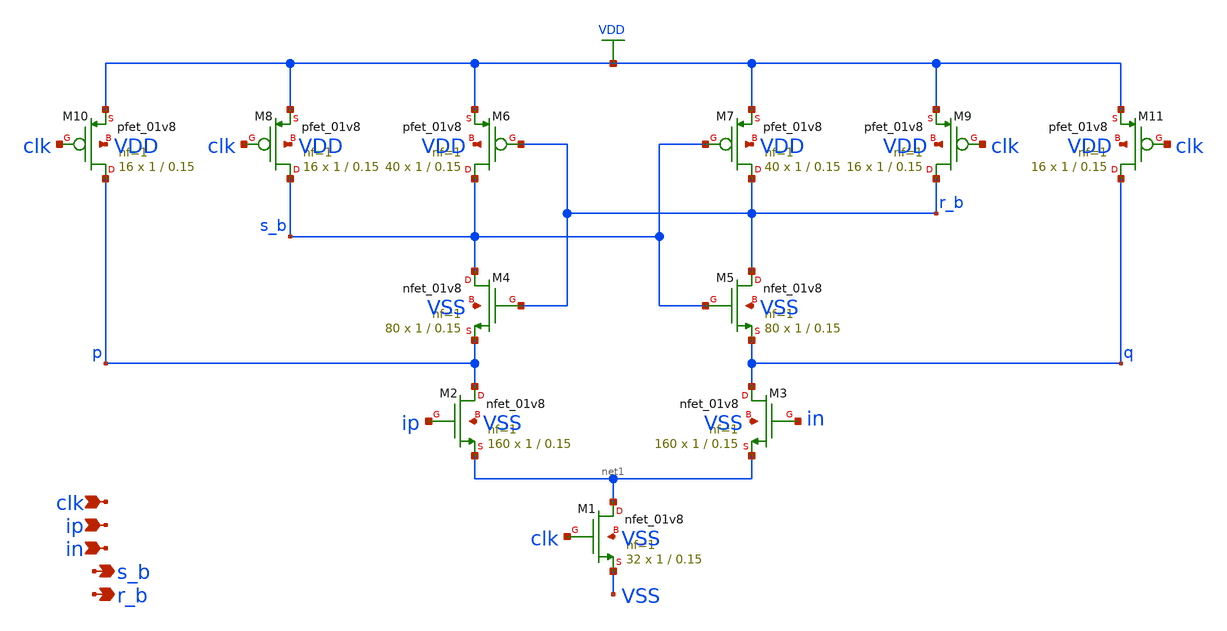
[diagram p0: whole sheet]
** sch_path: design/analog_modulator/schematic/comparator_core_large.sch
**.subckt comparator_core_large clk ip in s_b r_b
*.ipin clk
*.ipin ip
*.ipin in
*.opin s_b
*.opin r_b
XM1 net1 clk VSS VSS sky130_fd_pr__nfet_01v8 L=0.15 W=1 nf=1 ad='int((nf+1)/2) * W/nf * 0.29' as='int((nf+2)/2) * W/nf * 0.29'
+ pd='2*int((nf+1)/2) * (W/nf + 0.29)' ps='2*int((nf+2)/2) * (W/nf + 0.29)' nrd='0.29 / W' nrs='0.29 / W'
+ sa=0 sb=0 sd=0 mult=32 m=32
XM2 p ip net1 VSS sky130_fd_pr__nfet_01v8 L=0.15 W=1 nf=1 ad='int((nf+1)/2) * W/nf * 0.29' as='int((nf+2)/2) * W/nf * 0.29'
+ pd='2*int((nf+1)/2) * (W/nf + 0.29)' ps='2*int((nf+2)/2) * (W/nf + 0.29)' nrd='0.29 / W' nrs='0.29 / W'
+ sa=0 sb=0 sd=0 mult=160 m=160
XM3 q in net1 VSS sky130_fd_pr__nfet_01v8 L=0.15 W=1 nf=1 ad='int((nf+1)/2) * W/nf * 0.29' as='int((nf+2)/2) * W/nf * 0.29'
+ pd='2*int((nf+1)/2) * (W/nf + 0.29)' ps='2*int((nf+2)/2) * (W/nf + 0.29)' nrd='0.29 / W' nrs='0.29 / W'
+ sa=0 sb=0 sd=0 mult=160 m=160
XM4 s_b r_b p VSS sky130_fd_pr__nfet_01v8 L=0.15 W=1 nf=1 ad='int((nf+1)/2) * W/nf * 0.29' as='int((nf+2)/2) * W/nf * 0.29'
+ pd='2*int((nf+1)/2) * (W/nf + 0.29)' ps='2*int((nf+2)/2) * (W/nf + 0.29)' nrd='0.29 / W' nrs='0.29 / W'
+ sa=0 sb=0 sd=0 mult=80 m=80
XM5 r_b s_b q VSS sky130_fd_pr__nfet_01v8 L=0.15 W=1 nf=1 ad='int((nf+1)/2) * W/nf * 0.29' as='int((nf+2)/2) * W/nf * 0.29'
+ pd='2*int((nf+1)/2) * (W/nf + 0.29)' ps='2*int((nf+2)/2) * (W/nf + 0.29)' nrd='0.29 / W' nrs='0.29 / W'
+ sa=0 sb=0 sd=0 mult=80 m=80
XM6 s_b r_b VDD VDD sky130_fd_pr__pfet_01v8 L=0.15 W=1 nf=1 ad='int((nf+1)/2) * W/nf * 0.29' as='int((nf+2)/2) * W/nf * 0.29'
+ pd='2*int((nf+1)/2) * (W/nf + 0.29)' ps='2*int((nf+2)/2) * (W/nf + 0.29)' nrd='0.29 / W' nrs='0.29 / W'
+ sa=0 sb=0 sd=0 mult=40 m=40
XM7 r_b s_b VDD VDD sky130_fd_pr__pfet_01v8 L=0.15 W=1 nf=1 ad='int((nf+1)/2) * W/nf * 0.29' as='int((nf+2)/2) * W/nf * 0.29'
+ pd='2*int((nf+1)/2) * (W/nf + 0.29)' ps='2*int((nf+2)/2) * (W/nf + 0.29)' nrd='0.29 / W' nrs='0.29 / W'
+ sa=0 sb=0 sd=0 mult=40 m=40
XM8 s_b clk VDD VDD sky130_fd_pr__pfet_01v8 L=0.15 W=1 nf=1 ad='int((nf+1)/2) * W/nf * 0.29' as='int((nf+2)/2) * W/nf * 0.29'
+ pd='2*int((nf+1)/2) * (W/nf + 0.29)' ps='2*int((nf+2)/2) * (W/nf + 0.29)' nrd='0.29 / W' nrs='0.29 / W'
+ sa=0 sb=0 sd=0 mult=16 m=16
XM9 r_b clk VDD VDD sky130_fd_pr__pfet_01v8 L=0.15 W=1 nf=1 ad='int((nf+1)/2) * W/nf * 0.29' as='int((nf+2)/2) * W/nf * 0.29'
+ pd='2*int((nf+1)/2) * (W/nf + 0.29)' ps='2*int((nf+2)/2) * (W/nf + 0.29)' nrd='0.29 / W' nrs='0.29 / W'
+ sa=0 sb=0 sd=0 mult=16 m=16
XM10 p clk VDD VDD sky130_fd_pr__pfet_01v8 L=0.15 W=1 nf=1 ad='int((nf+1)/2) * W/nf * 0.29' as='int((nf+2)/2) * W/nf * 0.29'
+ pd='2*int((nf+1)/2) * (W/nf + 0.29)' ps='2*int((nf+2)/2) * (W/nf + 0.29)' nrd='0.29 / W' nrs='0.29 / W'
+ sa=0 sb=0 sd=0 mult=16 m=16
XM11 q clk VDD VDD sky130_fd_pr__pfet_01v8 L=0.15 W=1 nf=1 ad='int((nf+1)/2) * W/nf * 0.29' as='int((nf+2)/2) * W/nf * 0.29'
+ pd='2*int((nf+1)/2) * (W/nf + 0.29)' ps='2*int((nf+2)/2) * (W/nf + 0.29)' nrd='0.29 / W' nrs='0.29 / W'
+ sa=0 sb=0 sd=0 mult=16 m=16
**.ends
.GLOBAL VDD
.end
